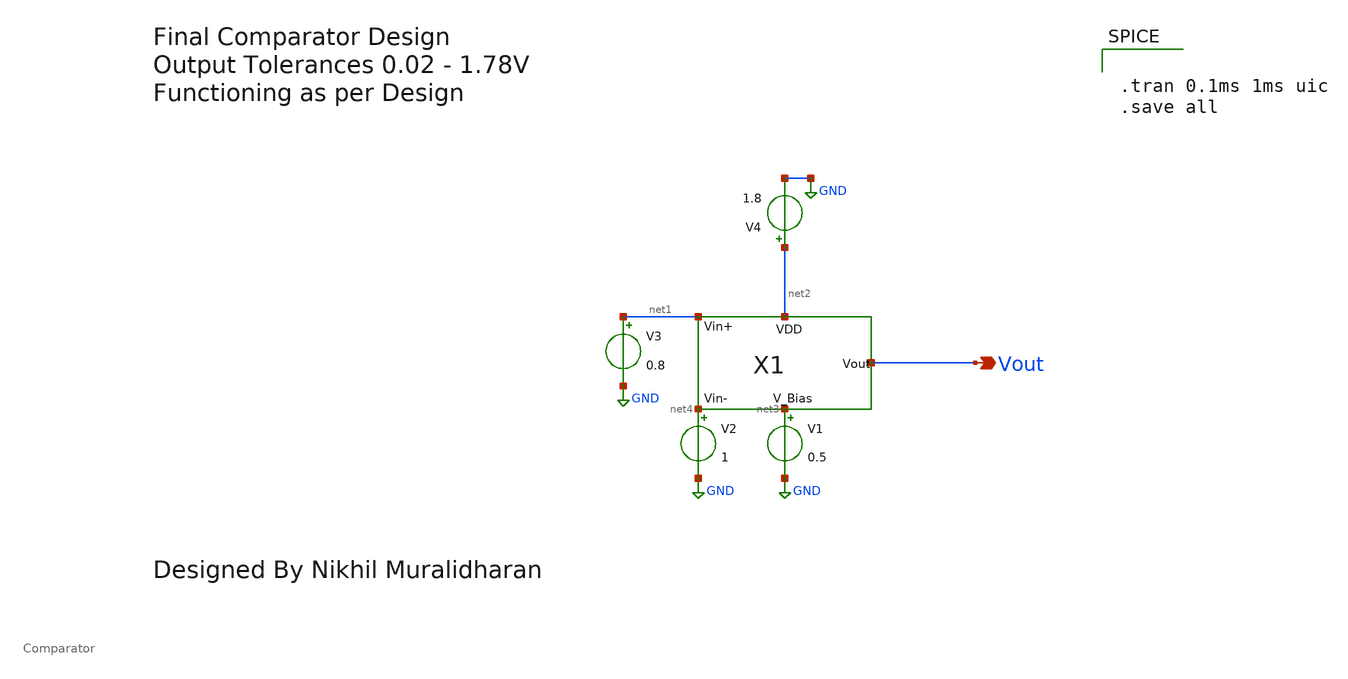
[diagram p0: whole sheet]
** sch_path: Current Sensor/comparator_testing.sch
**.subckt comparator_testing Vout
*.opin Vout
X1 net3 net1 net4 Vout net2 Comparator
V1 net3 GND 0.5
V4 net2 GND 1.8
V2 net4 GND 1
V3 net1 GND 0.8
**** begin user architecture code
** manual skywater pdks install (with patches applied)
* .lib $::SKYWATER_MODELS/models/sky130.lib.spice tt_mm

** opencircuitdesign pdks install
.lib $::SKYWATER_MODELS/sky130.lib.spice tt_mm




.tran 0.1ms 1ms uic
.save all

**** end user architecture code
**.ends

* expanding   symbol:  Comparator.sym # of pins=5
** sym_path: Current Sensor/Comparator.sym
** sch_path: Current Sensor/Comparator.sch
.subckt Comparator V_Bias Vin_Plus Vin_Minus Vout VDD
*.ipin V_Bias
*.ipin Vin_Plus
*.ipin Vin_Minus
*.opin Vout
*.ipin VDD
XM1 net1 net1 VDD VDD sky130_fd_pr__pfet_01v8_lvt L=0.45 W=1 nf=1 ad='int((nf+1)/2) * W/nf * 0.29' as='int((nf+2)/2) * W/nf * 0.29'
+ pd='2*int((nf+1)/2) * (W/nf + 0.29)' ps='2*int((nf+2)/2) * (W/nf + 0.29)' nrd='0.29 / W' nrs='0.29 / W'
+ sa=0 sb=0 sd=0 mult=1 m=1
XM2 net2 net1 VDD VDD sky130_fd_pr__pfet_01v8_lvt L=0.45 W=1 nf=1 ad='int((nf+1)/2) * W/nf * 0.29' as='int((nf+2)/2) * W/nf * 0.29'
+ pd='2*int((nf+1)/2) * (W/nf + 0.29)' ps='2*int((nf+2)/2) * (W/nf + 0.29)' nrd='0.29 / W' nrs='0.29 / W'
+ sa=0 sb=0 sd=0 mult=1 m=1
XM3 Vout net2 VDD VDD sky130_fd_pr__pfet_01v8_lvt L=0.45 W=1 nf=1 ad='int((nf+1)/2) * W/nf * 0.29' as='int((nf+2)/2) * W/nf * 0.29'
+ pd='2*int((nf+1)/2) * (W/nf + 0.29)' ps='2*int((nf+2)/2) * (W/nf + 0.29)' nrd='0.29 / W' nrs='0.29 / W'
+ sa=0 sb=0 sd=0 mult=1 m=1
XM4 net3 V_Bias GND GND sky130_fd_pr__nfet_01v8_lvt L=0.15 W=1 nf=1 ad='int((nf+1)/2) * W/nf * 0.29'
+ as='int((nf+2)/2) * W/nf * 0.29' pd='2*int((nf+1)/2) * (W/nf + 0.29)' ps='2*int((nf+2)/2) * (W/nf + 0.29)'
+ nrd='0.29 / W' nrs='0.29 / W' sa=0 sb=0 sd=0 mult=1 m=1
XM5 Vout V_Bias GND GND sky130_fd_pr__nfet_01v8_lvt L=0.15 W=1 nf=1 ad='int((nf+1)/2) * W/nf * 0.29'
+ as='int((nf+2)/2) * W/nf * 0.29' pd='2*int((nf+1)/2) * (W/nf + 0.29)' ps='2*int((nf+2)/2) * (W/nf + 0.29)'
+ nrd='0.29 / W' nrs='0.29 / W' sa=0 sb=0 sd=0 mult=1 m=1
XM6 net1 Vin_Minus net3 net3 sky130_fd_pr__nfet_01v8_lvt L=0.15 W=1 nf=1 ad='int((nf+1)/2) * W/nf * 0.29'
+ as='int((nf+2)/2) * W/nf * 0.29' pd='2*int((nf+1)/2) * (W/nf + 0.29)' ps='2*int((nf+2)/2) * (W/nf + 0.29)'
+ nrd='0.29 / W' nrs='0.29 / W' sa=0 sb=0 sd=0 mult=1 m=1
XM7 net2 Vin_Plus net3 net3 sky130_fd_pr__nfet_01v8_lvt L=0.15 W=1 nf=1 ad='int((nf+1)/2) * W/nf * 0.29'
+ as='int((nf+2)/2) * W/nf * 0.29' pd='2*int((nf+1)/2) * (W/nf + 0.29)' ps='2*int((nf+2)/2) * (W/nf + 0.29)'
+ nrd='0.29 / W' nrs='0.29 / W' sa=0 sb=0 sd=0 mult=1 m=1
.ends

.GLOBAL GND
.end
